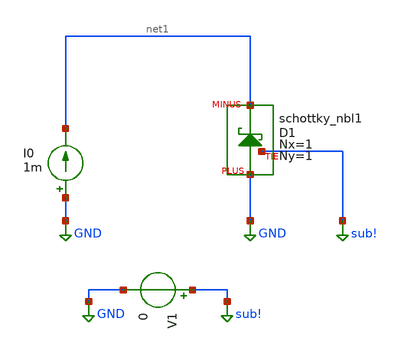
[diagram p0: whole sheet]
** sch_path: ihp-sg13g2/xschem_libs/sg13g2_tests_ase/dc_schottky/schematic/dc_schottky.sch
* Copyright 2023 IHP PDK Authors
**.subckt dc_schottky
I0 GND net1 1m
XD1 GND net1 sub! schottky_nbl1 Nx=1 Ny=1
V1 sub! GND 0
**.ends
.GLOBAL GND
.GLOBAL sub!
.end
